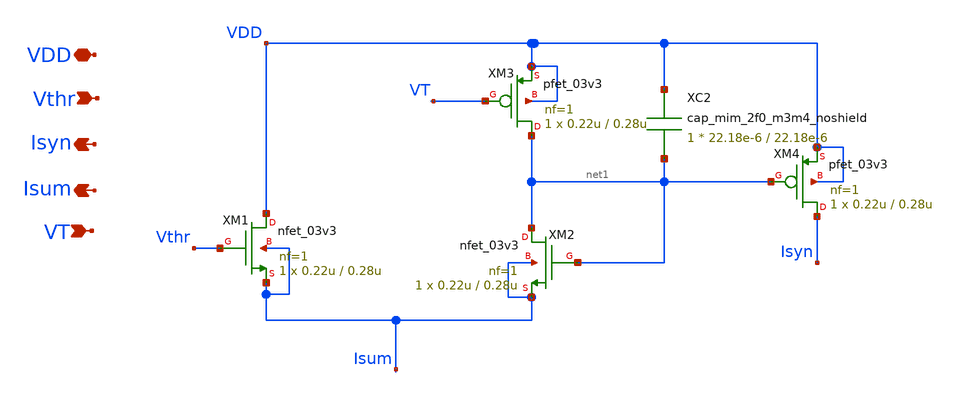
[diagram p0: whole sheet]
** sch_path: analog/DPI/DPI.sch
**.subckt DPI Vthr VDD Isyn Isum VT
*.ipin Vthr
*.iopin VDD
*.opin Isyn
*.opin Isum
*.ipin VT
XM1 VDD Vthr Isum Isum nfet_03v3 L=0.28u W=0.22u nf=1 ad='int((nf+1)/2) * W/nf * 0.18u' as='int((nf+2)/2) * W/nf * 0.18u'
+ pd='2*int((nf+1)/2) * (W/nf + 0.18u)' ps='2*int((nf+2)/2) * (W/nf + 0.18u)' nrd='0.18u / W' nrs='0.18u / W'
+ sa=0 sb=0 sd=0 m=1
XM2 net1 net1 Isum Isum nfet_03v3 L=0.28u W=0.22u nf=1 ad='int((nf+1)/2) * W/nf * 0.18u' as='int((nf+2)/2) * W/nf * 0.18u'
+ pd='2*int((nf+1)/2) * (W/nf + 0.18u)' ps='2*int((nf+2)/2) * (W/nf + 0.18u)' nrd='0.18u / W' nrs='0.18u / W'
+ sa=0 sb=0 sd=0 m=1
XM3 net1 VT VDD VDD pfet_03v3 L=0.28u W=0.22u nf=1 ad='int((nf+1)/2) * W/nf * 0.18u' as='int((nf+2)/2) * W/nf * 0.18u'
+ pd='2*int((nf+1)/2) * (W/nf + 0.18u)' ps='2*int((nf+2)/2) * (W/nf + 0.18u)' nrd='0.18u / W' nrs='0.18u / W'
+ sa=0 sb=0 sd=0 m=1
XM4 Isyn net1 VDD VDD pfet_03v3 L=0.28u W=0.22u nf=1 ad='int((nf+1)/2) * W/nf * 0.18u' as='int((nf+2)/2) * W/nf * 0.18u'
+ pd='2*int((nf+1)/2) * (W/nf + 0.18u)' ps='2*int((nf+2)/2) * (W/nf + 0.18u)' nrd='0.18u / W' nrs='0.18u / W'
+ sa=0 sb=0 sd=0 m=1
XC2 VDD net1 cap_mim_2f0_m3m4_noshield c_width=22.18e-6 c_length=22.18e-6 m=1
**.ends
.end
